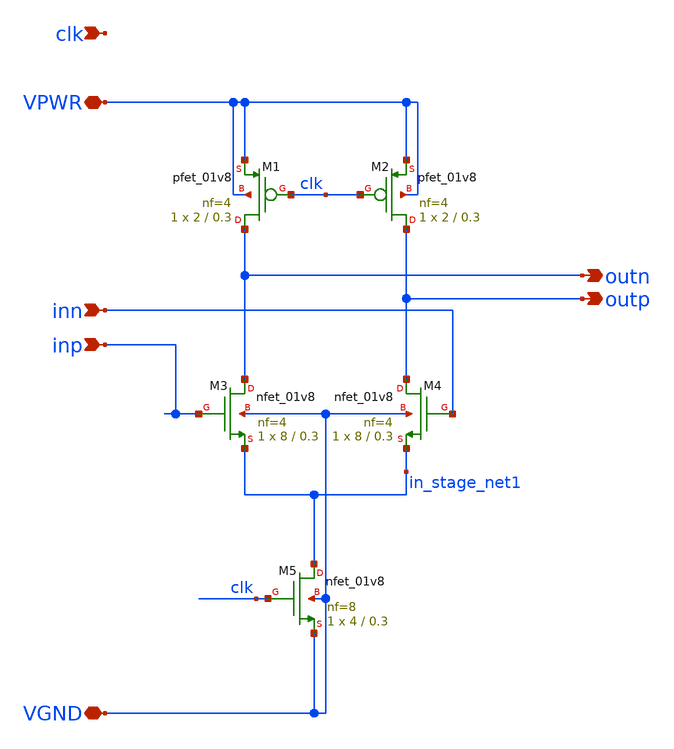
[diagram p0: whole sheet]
** sch_path: Circuits/Comparator/DiffAmp.sch
**.subckt DiffAmp VPWR VGND clk inp inn outn outp
*.iopin VPWR
*.iopin VGND
*.ipin clk
*.ipin inp
*.ipin inn
*.opin outn
*.opin outp
XM3 outn inp in_stage_net1 VGND sky130_fd_pr__nfet_01v8 L=0.3 W=8 nf=4 ad='int((nf+1)/2) * W/nf * 0.29'
+ as='int((nf+2)/2) * W/nf * 0.29' pd='2*int((nf+1)/2) * (W/nf + 0.29)' ps='2*int((nf+2)/2) * (W/nf + 0.29)'
+ nrd='0.29 / W' nrs='0.29 / W' sa=0 sb=0 sd=0 mult=1 m=1
XM4 outp inn in_stage_net1 VGND sky130_fd_pr__nfet_01v8 L=0.3 W=8 nf=4 ad='int((nf+1)/2) * W/nf * 0.29'
+ as='int((nf+2)/2) * W/nf * 0.29' pd='2*int((nf+1)/2) * (W/nf + 0.29)' ps='2*int((nf+2)/2) * (W/nf + 0.29)'
+ nrd='0.29 / W' nrs='0.29 / W' sa=0 sb=0 sd=0 mult=1 m=1
XM5 in_stage_net1 clk VGND VGND sky130_fd_pr__nfet_01v8 L=0.3 W=4 nf=8 ad='int((nf+1)/2) * W/nf * 0.29'
+ as='int((nf+2)/2) * W/nf * 0.29' pd='2*int((nf+1)/2) * (W/nf + 0.29)' ps='2*int((nf+2)/2) * (W/nf + 0.29)'
+ nrd='0.29 / W' nrs='0.29 / W' sa=0 sb=0 sd=0 mult=1 m=1
XM2 outp clk VPWR VPWR sky130_fd_pr__pfet_01v8 L=0.3 W=2 nf=4 ad='int((nf+1)/2) * W/nf * 0.29' as='int((nf+2)/2) * W/nf * 0.29'
+ pd='2*int((nf+1)/2) * (W/nf + 0.29)' ps='2*int((nf+2)/2) * (W/nf + 0.29)' nrd='0.29 / W' nrs='0.29 / W'
+ sa=0 sb=0 sd=0 mult=1 m=1
XM1 outn clk VPWR VPWR sky130_fd_pr__pfet_01v8 L=0.3 W=2 nf=4 ad='int((nf+1)/2) * W/nf * 0.29' as='int((nf+2)/2) * W/nf * 0.29'
+ pd='2*int((nf+1)/2) * (W/nf + 0.29)' ps='2*int((nf+2)/2) * (W/nf + 0.29)' nrd='0.29 / W' nrs='0.29 / W'
+ sa=0 sb=0 sd=0 mult=1 m=1
**.ends
.end
